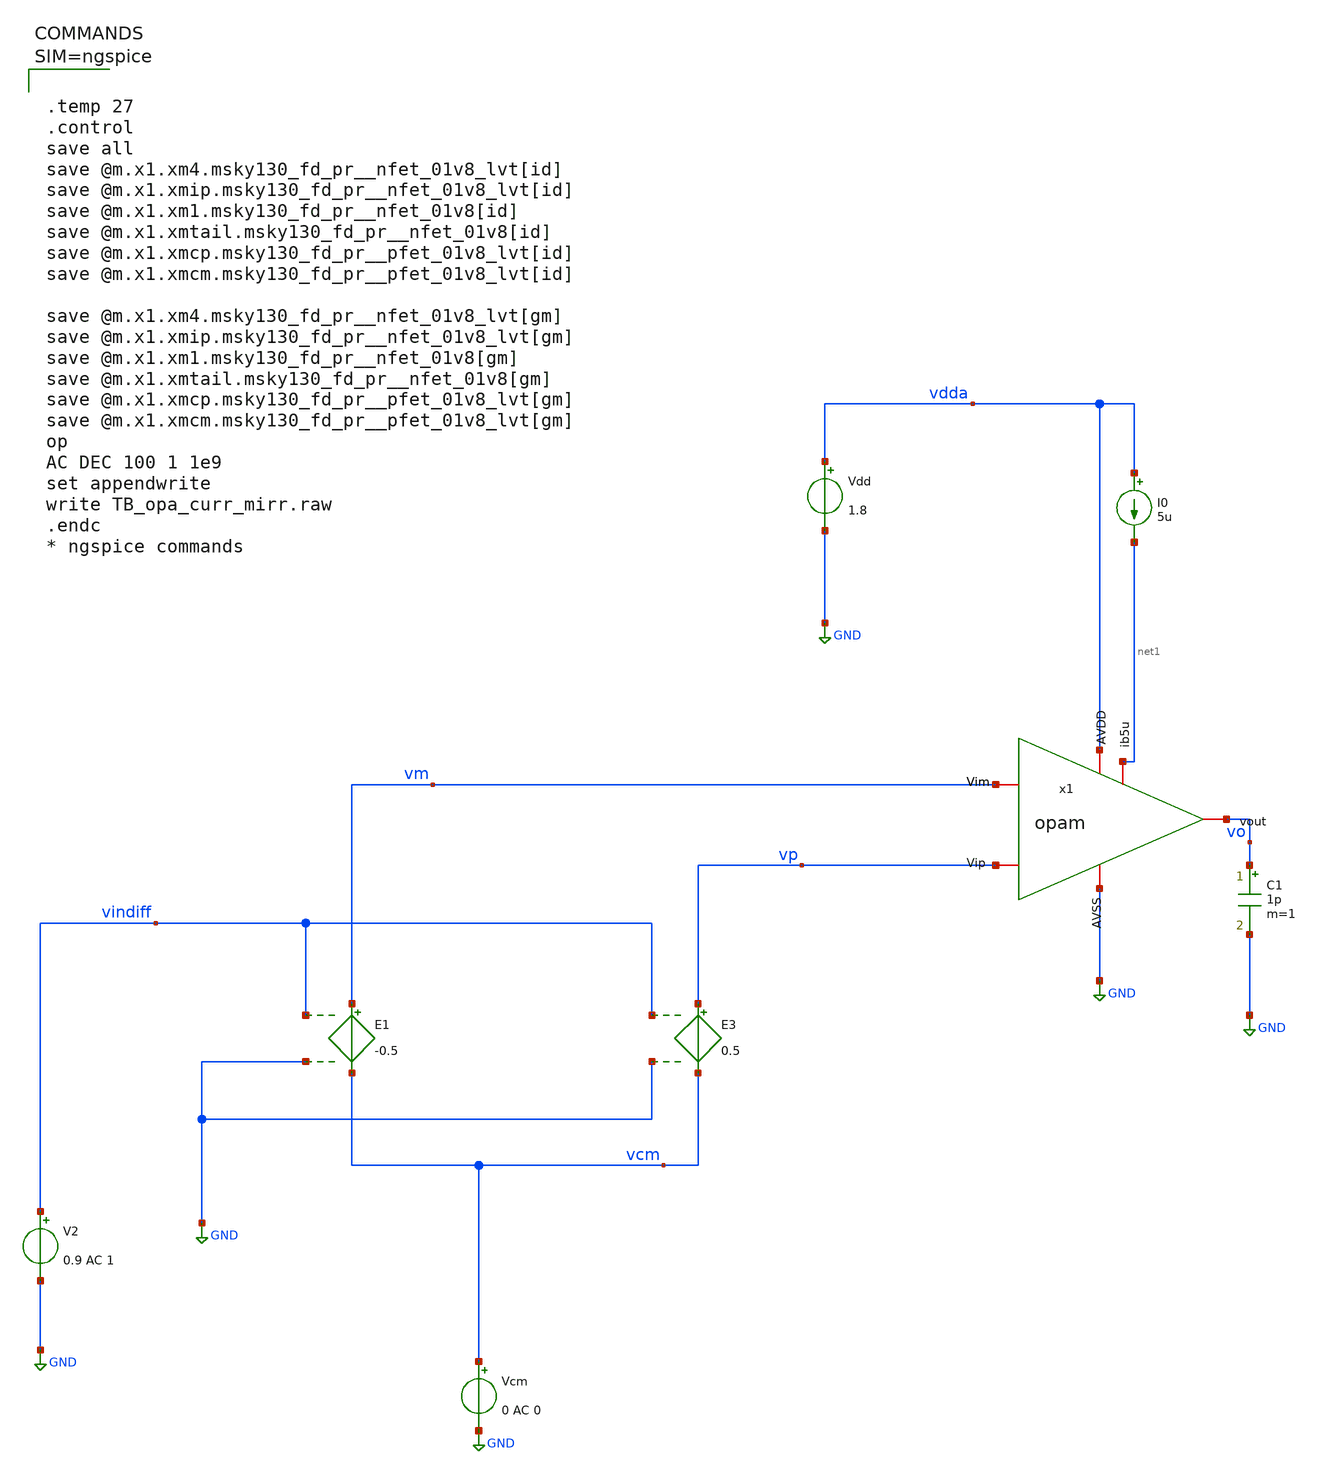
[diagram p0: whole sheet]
** sch_path: xschem/TB_opa_curr_mirr.sch
**.subckt TB_opa_curr_mirr
E1 vm vcm vindiff GND -0.5
E3 vp vcm vindiff GND 0.5
Vcm vcm GND 0 AC 0
V2 vindiff GND 0.9 AC 1
Vdd vdda GND 1.8
I0 vdda net1 5u
C1 vo GND 1p m=1
x1 vdda vo vm vp net1 GND opam
**** begin user architecture code

** opencircuitdesign pdks install
.lib $::SKYWATER_MODELS/sky130.lib.spice tt




.temp 27
.control
save all
save @m.x1.xm4.msky130_fd_pr__nfet_01v8_lvt[id]
save @m.x1.xmip.msky130_fd_pr__nfet_01v8_lvt[id]
save @m.x1.xm1.msky130_fd_pr__nfet_01v8[id]
save @m.x1.xmtail.msky130_fd_pr__nfet_01v8[id]
save @m.x1.xmcp.msky130_fd_pr__pfet_01v8_lvt[id]
save @m.x1.xmcm.msky130_fd_pr__pfet_01v8_lvt[id]

save @m.x1.xm4.msky130_fd_pr__nfet_01v8_lvt[gm]
save @m.x1.xmip.msky130_fd_pr__nfet_01v8_lvt[gm]
save @m.x1.xm1.msky130_fd_pr__nfet_01v8[gm]
save @m.x1.xmtail.msky130_fd_pr__nfet_01v8[gm]
save @m.x1.xmcp.msky130_fd_pr__pfet_01v8_lvt[gm]
save @m.x1.xmcm.msky130_fd_pr__pfet_01v8_lvt[gm]
op
AC DEC 100 1 1e9
set appendwrite
write TB_opa_curr_mirr.raw
.endc
* ngspice commands



**** end user architecture code
**.ends

* expanding   symbol:  opam.sym # of pins=6
** sym_path: xschem/opam.sym
** sch_path: xschem/opam.sch
.subckt opam AVDD vout Vim Vip ib5u AVSS
*.iopin AVSS
*.iopin ib5u
*.iopin AVDD
*.iopin Vip
*.iopin vout
*.iopin Vim
XMtail net1 ib5u AVSS AVSS sky130_fd_pr__nfet_01v8 L=1 W=5 nf=1 ad='int((1 + 1)/2) * 5 / 1 * 0.29' as='int((1 + 2)/2) * 5 / 1 * 0.29'
+ pd='2*int((1 + 1)/2) * (5 / 1 + 0.29)' ps='2*int((1 + 2)/2) * (5 / 1 + 0.29)' nrd='0.29 / 5 ' nrs='0.29 / 5 '
+ sa=0 sb=0 sd=0 mult=2 m=2
XM1 ib5u ib5u AVSS AVSS sky130_fd_pr__nfet_01v8 L=1 W=5 nf=1 ad='int((1 + 1)/2) * 5 / 1 * 0.29' as='int((1 + 2)/2) * 5 / 1 * 0.29'
+ pd='2*int((1 + 1)/2) * (5 / 1 + 0.29)' ps='2*int((1 + 2)/2) * (5 / 1 + 0.29)' nrd='0.29 / 5 ' nrs='0.29 / 5 '
+ sa=0 sb=0 sd=0 mult=1 m=1
XMip vom Vip net1 net1 sky130_fd_pr__nfet_01v8_lvt L=2 W=5 nf=1 ad='int((1 + 1)/2) * 5 / 1 * 0.29' as='int((1 + 2)/2) * 5 / 1 * 0.29'
+ pd='2*int((1 + 1)/2) * (5 / 1 + 0.29)' ps='2*int((1 + 2)/2) * (5 / 1 + 0.29)' nrd='0.29 / 5 ' nrs='0.29 / 5 '
+ sa=0 sb=0 sd=0 mult=4 m=4
XM4 vout Vim net1 net1 sky130_fd_pr__nfet_01v8_lvt L=2 W=5 nf=1 ad='int((1 + 1)/2) * 5 / 1 * 0.29' as='int((1 + 2)/2) * 5 / 1 * 0.29'
+ pd='2*int((1 + 1)/2) * (5 / 1 + 0.29)' ps='2*int((1 + 2)/2) * (5 / 1 + 0.29)' nrd='0.29 / 5 ' nrs='0.29 / 5 '
+ sa=0 sb=0 sd=0 mult=4 m=4
XMcp vom vom AVDD AVDD sky130_fd_pr__pfet_01v8_lvt L=2 W=5 nf=1 ad='int((1 + 1)/2) * 5 / 1 * 0.29' as='int((1 + 2)/2) * 5 / 1 * 0.29'
+ pd='2*int((1 + 1)/2) * (5 / 1 + 0.29)' ps='2*int((1 + 2)/2) * (5 / 1 + 0.29)' nrd='0.29 / 5 ' nrs='0.29 / 5 '
+ sa=0 sb=0 sd=0 mult=2 m=2
XMcm vout vom AVDD AVDD sky130_fd_pr__pfet_01v8_lvt L=2 W=5 nf=1 ad='int((1 + 1)/2) * 5 / 1 * 0.29' as='int((1 + 2)/2) * 5 / 1 * 0.29'
+ pd='2*int((1 + 1)/2) * (5 / 1 + 0.29)' ps='2*int((1 + 2)/2) * (5 / 1 + 0.29)' nrd='0.29 / 5 ' nrs='0.29 / 5 '
+ sa=0 sb=0 sd=0 mult=2 m=2
.ends

.GLOBAL GND
.end
